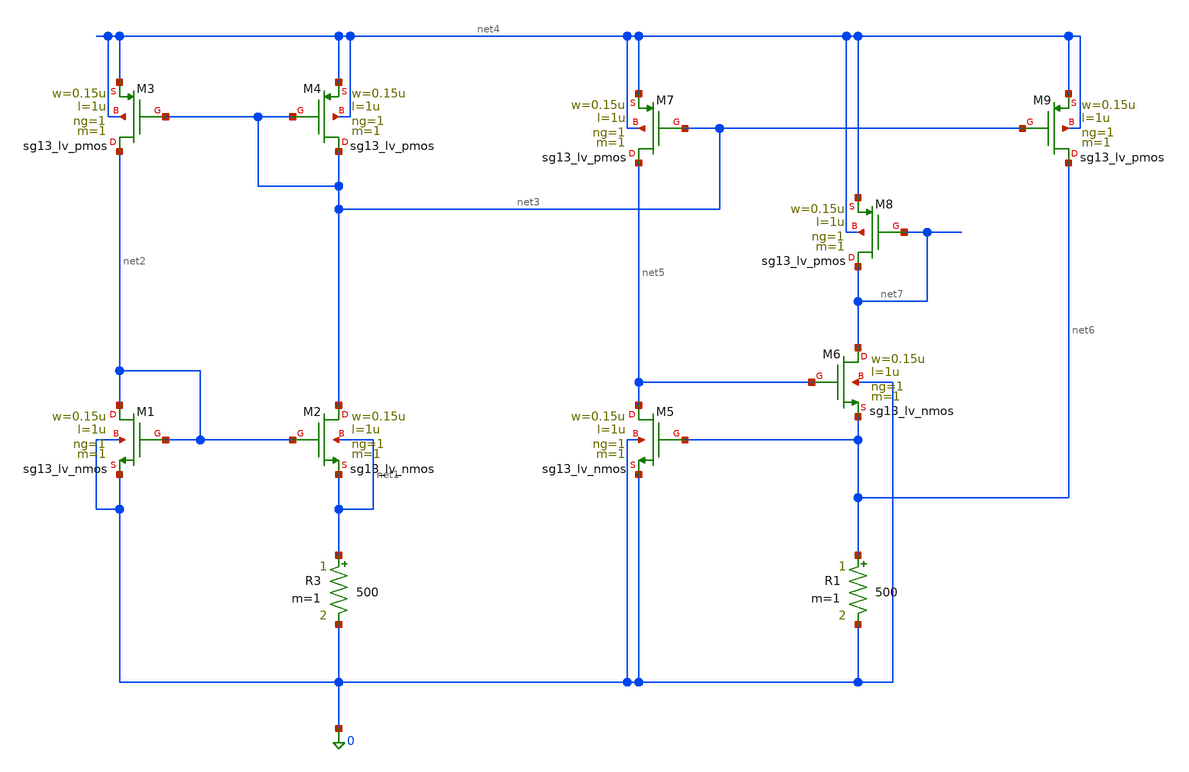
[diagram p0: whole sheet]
** sch_path: schematics/charge_pump/vbias/vbias_v4.sch
**.subckt vbias_v4
XM1 net2 net2 0 0 sg13_lv_nmos w=0.15u l=1u ng=1 m=1 mm_ok=1
XM3 net2 net3 net4 net4 sg13_lv_pmos w=0.15u l=1u ng=1 m=1 mm_ok=1
XM2 net3 net2 net1 net1 sg13_lv_nmos w=0.15u l=1u ng=1 m=1 mm_ok=1
XM4 net3 net3 net4 net4 sg13_lv_pmos w=0.15u l=1u ng=1 m=1 mm_ok=1
R3 net1 0 500 m=1
XM5 net5 net6 0 0 sg13_lv_nmos w=0.15u l=1u ng=1 m=1 mm_ok=1
XM6 net7 net5 net6 0 sg13_lv_nmos w=0.15u l=1u ng=1 m=1 mm_ok=1
R1 net6 0 500 m=1
XM7 net5 net3 net4 net4 sg13_lv_pmos w=0.15u l=1u ng=1 m=1 mm_ok=1
XM8 net7 net7 net4 net4 sg13_lv_pmos w=0.15u l=1u ng=1 m=1 mm_ok=1
XM9 net6 net3 net4 net4 sg13_lv_pmos w=0.15u l=1u ng=1 m=1 mm_ok=1
**.ends
.end
